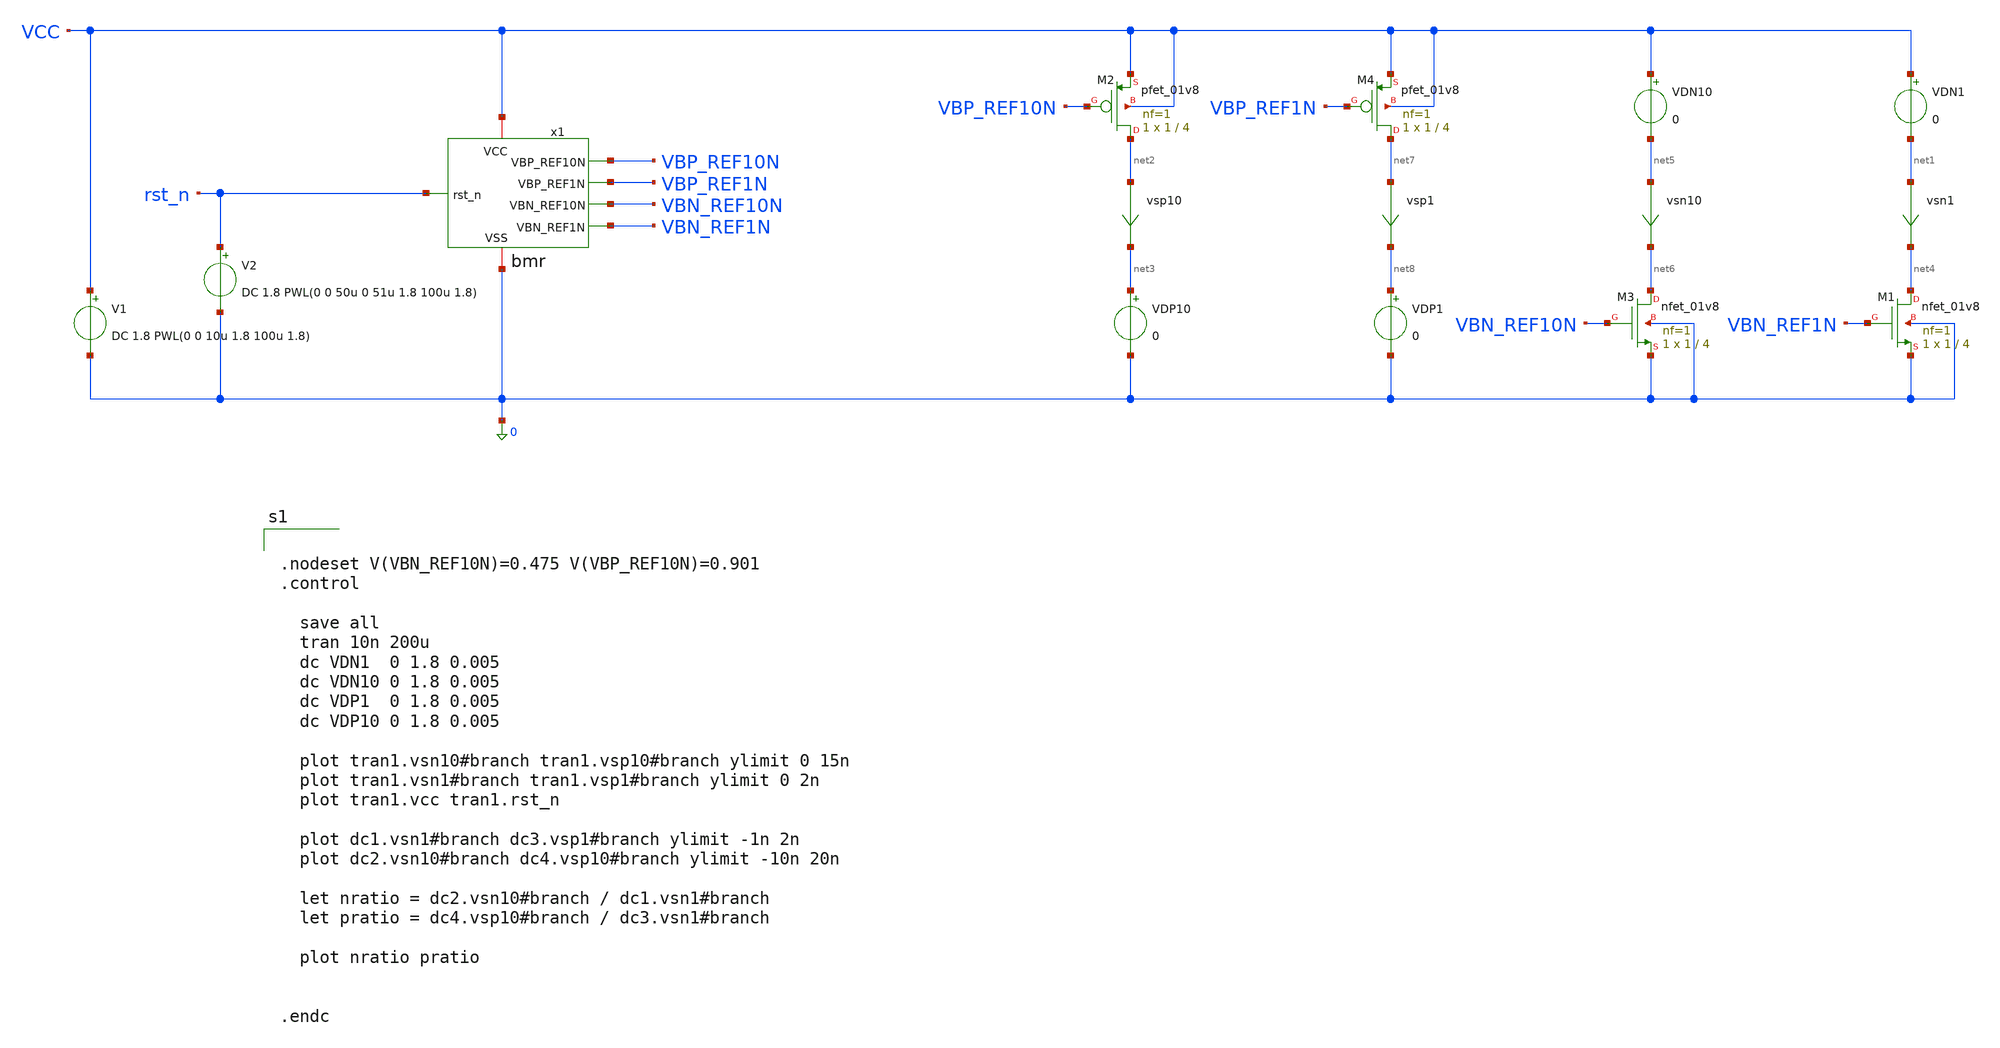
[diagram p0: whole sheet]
** sch_path: schem/bias/bmr_tb.sch
**.subckt bmr_tb
x1 VCC VBP_REF10N 0 VBP_REF1N VBN_REF10N VBN_REF1N rst_n bmr
vsn1 net1 net4 0
.save i(vsn1)
vsp10 net2 net3 0
.save i(vsp10)
XM1 net4 VBN_REF1N 0 0 sky130_fd_pr__nfet_01v8 L=4 W=1 nf=1 ad='int((1 + 1)/2) * 1 / 1 * 0.29' as='int((1 + 2)/2) * 1 / 1 * 0.29'
+ pd='2*int((1 + 1)/2) * (1 / 1 + 0.29)' ps='2*int((1 + 2)/2) * (1 / 1 + 0.29)' nrd='0.29 / 1 ' nrs='0.29 / 1 '
+ sa=0 sb=0 sd=0 mult=1 m=1
XM2 net2 VBP_REF10N VCC VCC sky130_fd_pr__pfet_01v8 L=4 W=1 nf=1 ad='int((1 + 1)/2) * 1 / 1 * 0.29' as='int((1 + 2)/2) * 1 / 1 * 0.29'
+ pd='2*int((1 + 1)/2) * (1 / 1 + 0.29)' ps='2*int((1 + 2)/2) * (1 / 1 + 0.29)' nrd='0.29 / 1 ' nrs='0.29 / 1 '
+ sa=0 sb=0 sd=0 mult=1 m=1
VDN1 VCC net1 0
VDP10 net3 0 0
vsn10 net5 net6 0
.save i(vsn10)
XM3 net6 VBN_REF10N 0 0 sky130_fd_pr__nfet_01v8 L=4 W=1 nf=1 ad='int((1 + 1)/2) * 1 / 1 * 0.29' as='int((1 + 2)/2) * 1 / 1 * 0.29'
+ pd='2*int((1 + 1)/2) * (1 / 1 + 0.29)' ps='2*int((1 + 2)/2) * (1 / 1 + 0.29)' nrd='0.29 / 1 ' nrs='0.29 / 1 '
+ sa=0 sb=0 sd=0 mult=1 m=1
VDN10 VCC net5 0
vsp1 net7 net8 0
.save i(vsp1)
XM4 net7 VBP_REF1N VCC VCC sky130_fd_pr__pfet_01v8 L=4 W=1 nf=1 ad='int((1 + 1)/2) * 1 / 1 * 0.29' as='int((1 + 2)/2) * 1 / 1 * 0.29'
+ pd='2*int((1 + 1)/2) * (1 / 1 + 0.29)' ps='2*int((1 + 2)/2) * (1 / 1 + 0.29)' nrd='0.29 / 1 ' nrs='0.29 / 1 '
+ sa=0 sb=0 sd=0 mult=1 m=1
VDP1 net8 0 0
V1 VCC 0 DC 1.8 PWL(0 0 10u 1.8 100u 1.8)
V2 rst_n 0 DC 1.8 PWL(0 0 50u 0 51u 1.8 100u 1.8)
**** begin user architecture code

** opencircuitdesign pdks install
.lib $::SKYWATER_MODELS/sky130.lib.spice tt



.nodeset V(VBN_REF10N)=0.475 V(VBP_REF10N)=0.901
.control

  save all
  tran 10n 200u
  dc VDN1  0 1.8 0.005
  dc VDN10 0 1.8 0.005
  dc VDP1  0 1.8 0.005
  dc VDP10 0 1.8 0.005

  plot tran1.vsn10#branch tran1.vsp10#branch ylimit 0 15n
  plot tran1.vsn1#branch tran1.vsp1#branch ylimit 0 2n
  plot tran1.vcc tran1.rst_n

  plot dc1.vsn1#branch dc3.vsp1#branch ylimit -1n 2n
  plot dc2.vsn10#branch dc4.vsp10#branch ylimit -10n 20n

  let nratio = dc2.vsn10#branch / dc1.vsn1#branch
  let pratio = dc4.vsp10#branch / dc3.vsn1#branch

  plot nratio pratio


.endc


**** end user architecture code
**.ends

* expanding   symbol:  bmr.sym # of pins=7
** sym_path: schem/bias/bmr.sym
** sch_path: schem/bias/bmr.sch
.subckt bmr VCC VBP_REF10N VSS VBP_REF1N VBN_REF10N VBN_REF1N rst_n
*.iopin VCC
*.iopin VSS
*.ipin rst_n
*.opin VBP_REF10N
*.opin VBP_REF1N
*.opin VBN_REF10N
*.opin VBN_REF1N
x1 VCC VBP_REF10N VSS VBN_REF10N rst_n bmr_10n
XM1 net1 VBP_REF10N VCC VCC sky130_fd_pr__pfet_01v8 L=4 W=1 nf=1 ad='int((1 + 1)/2) * 1 / 1 * 0.29' as='int((1 + 2)/2) * 1 / 1 * 0.29'
+ pd='2*int((1 + 1)/2) * (1 / 1 + 0.29)' ps='2*int((1 + 2)/2) * (1 / 1 + 0.29)' nrd='0.29 / 1 ' nrs='0.29 / 1 '
+ sa=0 sb=0 sd=0 mult=1 m=1
XM2 VBN_REF1N VBN_REF1N VSS VSS sky130_fd_pr__nfet_01v8 L=4 W=1 nf=1 ad='int((1 + 1)/2) * 1 / 1 * 0.29'
+ as='int((1 + 2)/2) * 1 / 1 * 0.29' pd='2*int((1 + 1)/2) * (1 / 1 + 0.29)' ps='2*int((1 + 2)/2) * (1 / 1 + 0.29)'
+ nrd='0.29 / 1 ' nrs='0.29 / 1 ' sa=0 sb=0 sd=0 mult=10 m=10
XM3 net2 VBN_REF1N VSS VSS sky130_fd_pr__nfet_01v8 L=4 W=1 nf=1 ad='int((1 + 1)/2) * 1 / 1 * 0.29' as='int((1 + 2)/2) * 1 / 1 * 0.29'
+ pd='2*int((1 + 1)/2) * (1 / 1 + 0.29)' ps='2*int((1 + 2)/2) * (1 / 1 + 0.29)' nrd='0.29 / 1 ' nrs='0.29 / 1 '
+ sa=0 sb=0 sd=0 mult=1 m=1
XM4 VBP_REF1N VBP_REF1N VCC VCC sky130_fd_pr__pfet_01v8 L=4 W=1 nf=1 ad='int((1 + 1)/2) * 1 / 1 * 0.29'
+ as='int((1 + 2)/2) * 1 / 1 * 0.29' pd='2*int((1 + 1)/2) * (1 / 1 + 0.29)' ps='2*int((1 + 2)/2) * (1 / 1 + 0.29)'
+ nrd='0.29 / 1 ' nrs='0.29 / 1 ' sa=0 sb=0 sd=0 mult=1 m=1
Vmeas net1 VBN_REF1N 0
.save i(vmeas)
Vmeas1 VBP_REF1N net2 0
.save i(vmeas1)
.ends


* expanding   symbol:  bias/bmr_10n.sym # of pins=5
** sym_path: schem/bias/bmr_10n.sym
** sch_path: schem/bias/bmr_10n.sch
.subckt bmr_10n VCC VBP VSS VBN rst_n
*.iopin VCC
*.iopin VSS
*.ipin rst_n
*.opin VBP
*.opin VBN
XM1 VBP VBP VCC VCC sky130_fd_pr__pfet_01v8 L=4 W=1 nf=1 ad='int((1 + 1)/2) * 1 / 1 * 0.29' as='int((1 + 2)/2) * 1 / 1 * 0.29'
+ pd='2*int((1 + 1)/2) * (1 / 1 + 0.29)' ps='2*int((1 + 2)/2) * (1 / 1 + 0.29)' nrd='0.29 / 1 ' nrs='0.29 / 1 '
+ sa=0 sb=0 sd=0 mult=1 m=1
XM2 net3 VBP VCC VCC sky130_fd_pr__pfet_01v8 L=4 W=1 nf=1 ad='int((1 + 1)/2) * 1 / 1 * 0.29' as='int((1 + 2)/2) * 1 / 1 * 0.29'
+ pd='2*int((1 + 1)/2) * (1 / 1 + 0.29)' ps='2*int((1 + 2)/2) * (1 / 1 + 0.29)' nrd='0.29 / 1 ' nrs='0.29 / 1 '
+ sa=0 sb=0 sd=0 mult=1 m=1
XM3 net2 VBN net1 VSS sky130_fd_pr__nfet_01v8 L=4 W=8 nf=1 ad='int((1 + 1)/2) * 8 / 1 * 0.29' as='int((1 + 2)/2) * 8 / 1 * 0.29'
+ pd='2*int((1 + 1)/2) * (8 / 1 + 0.29)' ps='2*int((1 + 2)/2) * (8 / 1 + 0.29)' nrd='0.29 / 8 ' nrs='0.29 / 8 '
+ sa=0 sb=0 sd=0 mult=1 m=1
XM4 VBN VBN VSS VSS sky130_fd_pr__nfet_01v8 L=4 W=1 nf=1 ad='int((1 + 1)/2) * 1 / 1 * 0.29' as='int((1 + 2)/2) * 1 / 1 * 0.29'
+ pd='2*int((1 + 1)/2) * (1 / 1 + 0.29)' ps='2*int((1 + 2)/2) * (1 / 1 + 0.29)' nrd='0.29 / 1 ' nrs='0.29 / 1 '
+ sa=0 sb=0 sd=0 mult=1 m=1
XR1 net5 net1 net4 sky130_fd_pr__res_xhigh_po_0p35 L={LR} mult=1 m=1
VSRIGHT VBP net2 0
.save i(vsright)
VSLEFT net3 VBN 0
.save i(vsleft)
XM5 VBN rst_n VCC VCC sky130_fd_pr__pfet_01v8 L=4 W=1 nf=1 ad='int((1 + 1)/2) * 1 / 1 * 0.29' as='int((1 + 2)/2) * 1 / 1 * 0.29'
+ pd='2*int((1 + 1)/2) * (1 / 1 + 0.29)' ps='2*int((1 + 2)/2) * (1 / 1 + 0.29)' nrd='0.29 / 1 ' nrs='0.29 / 1 '
+ sa=0 sb=0 sd=0 mult=1 m=1
XR2 net6 net5 net4 sky130_fd_pr__res_xhigh_po_0p35 L={LR} mult=1 m=1
XR3 net7 net6 net4 sky130_fd_pr__res_xhigh_po_0p35 L={LR} mult=1 m=1
XR4 net8 net7 net4 sky130_fd_pr__res_xhigh_po_0p35 L={LR} mult=1 m=1
XR5 net9 net8 net4 sky130_fd_pr__res_xhigh_po_0p35 L={LR} mult=1 m=1
XR6 net10 net9 net4 sky130_fd_pr__res_xhigh_po_0p35 L={LR} mult=1 m=1
XR7 net11 net10 net4 sky130_fd_pr__res_xhigh_po_0p35 L={LR} mult=1 m=1
XR8 VSS net11 net4 sky130_fd_pr__res_xhigh_po_0p35 L={LR} mult=1 m=1
**** begin user architecture code


.param LR=1084/8


**** end user architecture code
.ends

.end
